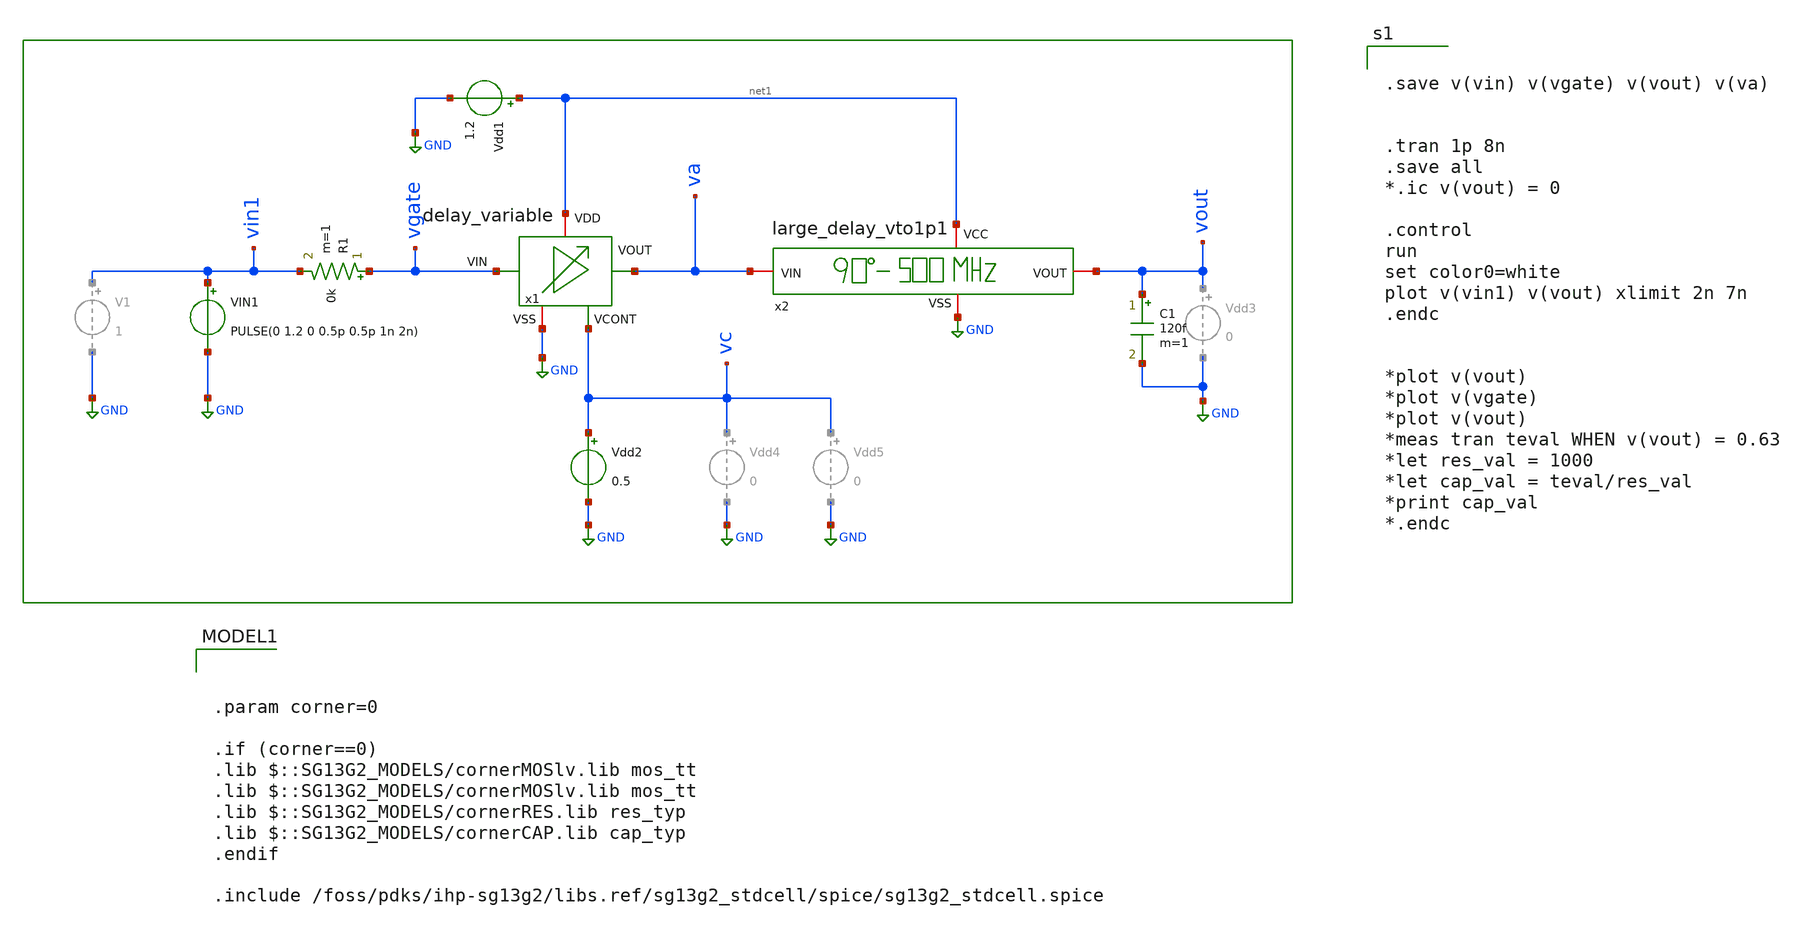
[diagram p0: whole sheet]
** sch_path: sch/delay_variable_line/tb_QVDL_500MHZ.sch
* IHP-GmbH/IHP-Open-PDK/ihp-sg13g2/libs.tech/xschem/sg13g2_stdcells/sg13g2_dlygate4sd2_1.sch:
* Copyright 2023 IHP PDK Authors
* Licensed under the Apache License, Version 2.0 (the "License");
**.subckt tb_QVDL_500MHZ
R1 vgate vin1 0k m=1
Vdd1 net1 GND 1.2
Vdd2 vc GND 0.5
C1 vout GND 120f m=1
VIN1 vin1 GND PULSE(0 1.2 0 0.5p 0.5p 1n 2n)
x2 net1 GND va vout large_delay_vto1p1
x1 net1 vgate va vc GND delay_variable
**** begin user architecture code


.save v(vin) v(vgate) v(vout) v(va)


.tran 1p 8n
.save all
*.ic v(vout) = 0

.control
run
set color0=white
plot v(vin1) v(vout) xlimit 2n 7n
.endc


*plot v(vout)
*plot v(vgate)
*plot v(vout)
*meas tran teval WHEN v(vout) = 0.63
*let res_val = 1000
*let cap_val = teval/res_val
*print cap_val
*.endc




.param corner=0

.if (corner==0)
.lib $::SG13G2_MODELS/cornerMOSlv.lib mos_tt
.lib $::SG13G2_MODELS/cornerMOSlv.lib mos_tt
.lib $::SG13G2_MODELS/cornerRES.lib res_typ
.lib $::SG13G2_MODELS/cornerCAP.lib cap_typ
.endif

.include /foss/pdks/ihp-sg13g2/libs.ref/sg13g2_stdcell/spice/sg13g2_stdcell.spice

**** end user architecture code
**.ends

* expanding   symbol:  /foss/designs/UNIC-CASS-Aug25/sch/large_delay_vto1p1/large_delay_vto1p1.sym #
*+ of pins=4
** sym_path: sch/large_delay_vto1p1/large_delay_vto1p1.sym
** sch_path: sch/large_delay_vto1p1/large_delay_vto1p1.sch
.subckt large_delay_vto1p1 VCC VSS VIN VOUT
*.iopin VIN
*.iopin VOUT
*.iopin VCC
*.iopin VSS
x1 net1 VIN VCC VSS sg13g2_dlygate4sd2_1
x2 net1 VIN VCC VSS sg13g2_dlygate4sd2_1
x3 net1 VIN VCC VSS sg13g2_dlygate4sd2_1
x4 net1 VIN VCC VSS sg13g2_dlygate4sd3_1
x6 VOUT net1 VCC VSS sg13g2_dlygate4sd1_1
x7 VOUT net1 VCC VSS sg13g2_dlygate4sd1_1
x8 VOUT net1 VCC VSS sg13g2_dlygate4sd1_1
x9 VOUT net1 VCC VSS sg13g2_dlygate4sd1_1
x10 net1 VIN VCC VSS sg13g2_dlygate4sd3_1
x11 VOUT net1 VCC VSS sg13g2_dlygate4sd3_1
.ends


* expanding   symbol:  /foss/designs/UNIC-CASS-Aug25/sch/delay_variable/delay_variable.sym # of
*+ pins=5
** sym_path: PhaseInterpolator/2to4/delay_variable.sym
** sch_path: PhaseInterpolator/2to4/delay_variable.sch
.subckt delay_variable VDD VIN VOUT VCONT VSS
*.iopin VSS
*.iopin VDD
*.opin VOUT
*.ipin VCONT
*.ipin VIN
XM1 VOUT VIN net2 VSS sg13_lv_nmos w=0.15u l=0.13u ng=1 m=4 mm_ok=1
XM2 net2 VCONT VSS VSS sg13_lv_nmos w=0.15u l=0.25u ng=1 m=2 mm_ok=1
XM3 net3 VCONT VSS VSS sg13_lv_nmos w=0.15u l=0.25u ng=1 m=1 mm_ok=1
XM5 VOUT VIN net1 VDD sg13_lv_pmos w=0.15u l=0.13u ng=1 m=4 mm_ok=1
XM6 net1 net3 VDD VDD sg13_lv_pmos w=0.15u l=0.25u ng=1 m=2 mm_ok=1
XM4 net3 net3 VDD VDD sg13_lv_pmos w=0.15u l=0.25u ng=1 m=1 mm_ok=1
.ends


* expanding   symbol:  sg13g2_stdcells/sg13g2_dlygate4sd3_1.sym # of pins=2
** sym_path: sg13g2_stdcells/sg13g2_dlygate4sd3_1.sym
** sch_path: sg13g2_stdcells/sg13g2_dlygate4sd3_1.sch
.subckt sg13g2_dlygate4sd3_1 X A VDD VSS
*.ipin A
*.opin X
*.iopin VDD
*.iopin VSS
XM1 net3 A VSS VSS sg13_lv_nmos w=420.00n l=130.00n ng=1 m=1 mm_ok=1
XM2 net1 net3 VSS VSS sg13_lv_nmos w=420.00n l=500.0n ng=1 m=1 mm_ok=1
XM3 net2 net1 VSS VSS sg13_lv_nmos w=420.00n l=500.0n ng=1 m=1 mm_ok=1
XM4 X net2 VSS VSS sg13_lv_nmos w=740.00n l=130.00n ng=1 m=1 mm_ok=1
XM5 net3 A VDD VDD sg13_lv_pmos w=420.00n l=130.00n ng=1 m=1 mm_ok=1
XM6 net1 net3 VDD VDD sg13_lv_pmos w=1.000u l=500.0n ng=1 m=1 mm_ok=1
XM7 net2 net1 VDD VDD sg13_lv_pmos w=1.000u l=500.0n ng=1 m=1 mm_ok=1
XM8 X net2 VDD VDD sg13_lv_pmos w=1.12u l=130.00n ng=1 m=1 mm_ok=1
.ends


* expanding   symbol:  sg13g2_stdcells/sg13g2_dlygate4sd2_1.sym # of pins=2
** sym_path: sg13g2_stdcells/sg13g2_dlygate4sd2_1.sym
** sch_path: sg13g2_stdcells/sg13g2_dlygate4sd2_1.sch
.subckt sg13g2_dlygate4sd2_1 X A VDD VSS
*.ipin A
*.opin X
*.iopin VDD
*.iopin VSS
XM1 net2 A VSS VSS sg13_lv_nmos w=420.00n l=130.00n ng=1 m=1 mm_ok=1
XM2 net1 net2 VSS VSS sg13_lv_nmos w=420.00n l=180.00n ng=1 m=1 mm_ok=1
XM3 net3 net1 VSS VSS sg13_lv_nmos w=420.00n l=180.00n ng=1 m=1 mm_ok=1
XM4 X net3 VSS VSS sg13_lv_nmos w=740.00n l=130.00n ng=1 m=1 mm_ok=1
XM5 net2 A VDD VDD sg13_lv_pmos w=420.00n l=130.00n ng=1 m=1 mm_ok=1
XM6 net1 net2 VDD VDD sg13_lv_pmos w=1.000u l=250.00n ng=1 m=1 mm_ok=1
XM7 net3 net1 VDD VDD sg13_lv_pmos w=1.000u l=250.00n ng=1 m=1 mm_ok=1
XM8 X net3 VDD VDD sg13_lv_pmos w=1.12u l=130.00n ng=1 m=1 mm_ok=1
.ends


* expanding   symbol:  sg13g2_stdcells/sg13g2_dlygate4sd1_1.sym # of pins=2
** sym_path: sg13g2_stdcells/sg13g2_dlygate4sd1_1.sym
** sch_path: sg13g2_stdcells/sg13g2_dlygate4sd1_1.sch
.subckt sg13g2_dlygate4sd1_1 X A VDD VSS
*.ipin A
*.opin X
*.iopin VDD
*.iopin VSS
XM1 net2 A VSS VSS sg13_lv_nmos w=420.00n l=130.00n ng=1 m=1 mm_ok=1
XM2 net1 net2 VSS VSS sg13_lv_nmos w=420.00n l=130.00n ng=1 m=1 mm_ok=1
XM3 net3 net1 VSS VSS sg13_lv_nmos w=420.00n l=130.00n ng=1 m=1 mm_ok=1
XM4 X net3 VSS VSS sg13_lv_nmos w=740.00n l=130.00n ng=1 m=1 mm_ok=1
XM5 net2 A VDD VDD sg13_lv_pmos w=420.00n l=130.00n ng=1 m=1 mm_ok=1
XM6 net1 net2 VDD VDD sg13_lv_pmos w=1.000u l=130.00n ng=1 m=1 mm_ok=1
XM7 net3 net1 VDD VDD sg13_lv_pmos w=1.000u l=130.00n ng=1 m=1 mm_ok=1
XM8 X net3 VDD VDD sg13_lv_pmos w=1.12u l=130.00n ng=1 m=1 mm_ok=1
.ends

.GLOBAL GND
.end
